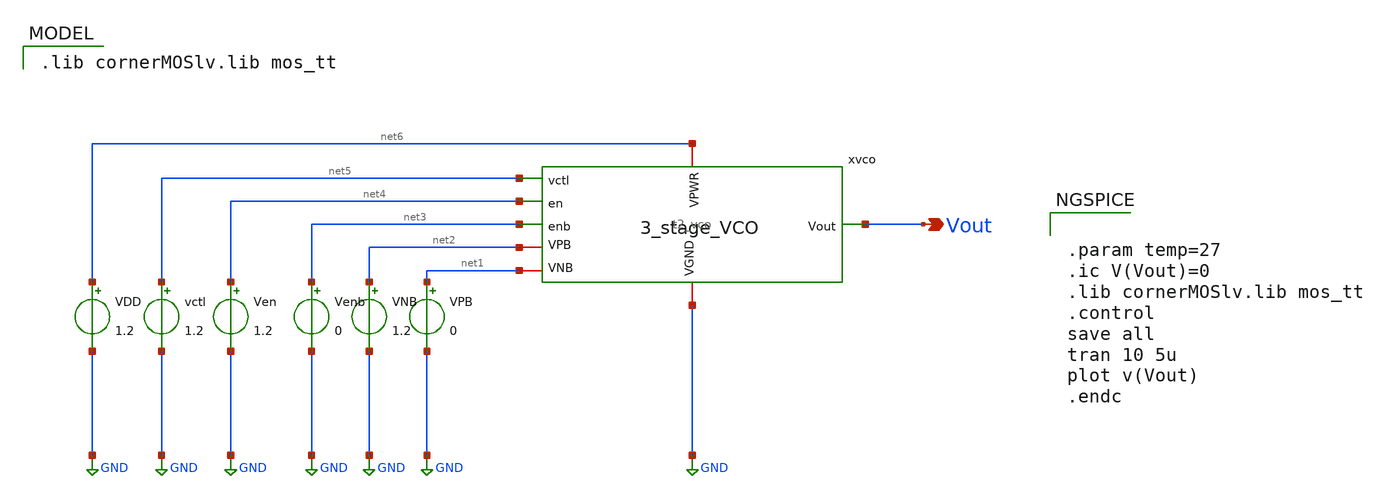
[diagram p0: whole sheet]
** sch_path: Team 2 Design/design_data/xschem/t2_vco_tb.sch
* IHP-GmbH/IHP-Open-PDK/ihp-sg13g2/libs.tech/xschem/sg13g2_stdcells/sg13g2_buf_1.sch:
* Copyright 2023 IHP PDK Authors
* Licensed under the Apache License, Version 2.0 (the "License");
**.subckt t2_vco_tb Vout
*.opin Vout
VDD net6 GND 1.2
vctl net5 GND 1.2
Ven net4 GND 1.2
Venb net3 GND 0
VNB net2 GND 1.2
VPB net1 GND 0
x1 net6 net2 GND net1 Vout net5 net4 net3 t2_vco
**** begin user architecture code
 .lib cornerMOSlv.lib mos_tt



.param temp=27
.ic V(Vout)=0
.lib cornerMOSlv.lib mos_tt
.control
save all
tran 10 5u
plot v(Vout)
.endc


**** end user architecture code
**.ends

* expanding   symbol:  /foss/designs/cmos-pll-ihp-sg13g2/Team 2 Design/design_data/xschem/t2_vco.sym
*+ # of pins=8
** sym_path: Team 2 Design/design_data/xschem/t2_vco.sym
** sch_path: Team 2 Design/design_data/xschem/t2_vco.sch
.subckt t2_vco VPWR VPB VGND VNB Vout vctl en enb
*.iopin VPWR
*.iopin VPB
*.iopin VGND
*.iopin VNB
*.ipin vctl
*.ipin en
*.ipin enb
*.opin Vout
XM1 net1 en VPWR VPB sg13_lv_pmos w=1.0u l=0.15u ng=1 m=1 mm_ok=1
XM2 net1 net1 VPWR VPB sg13_lv_pmos w=3.0u l=0.15u ng=1 m=1 mm_ok=1
XM3 vco_source net1 VPWR VPB sg13_lv_pmos w=3.0u l=0.15u ng=1 m=1 mm_ok=1
XM4 net1 vctl net2 VNB sg13_lv_nmos w=1.5u l=0.15u ng=1 m=1 mm_ok=1
XM5 net2 net2 VGND VNB sg13_lv_nmos w=1.5u l=0.15u ng=1 m=1 mm_ok=1
XM6 vco_sink net2 VGND VNB sg13_lv_nmos w=1.5u l=0.15u ng=1 m=1 mm_ok=1
XM7 net2 enb VGND VNB sg13_lv_nmos w=0.5u l=0.15u ng=1 m=1 mm_ok=1
XM8 vctl enb VGND VNB sg13_lv_nmos w=0.5u l=0.15u ng=1 m=1 mm_ok=1
XM9 net3 enb VGND VNB sg13_lv_nmos w=0.5u l=0.15u ng=1 m=1 mm_ok=1
x2 vco_source net3 net4 vco_sink t2_inverter
x3 vco_source net4 net5 vco_sink t2_inverter
x4 vco_source net5 net3 vco_sink t2_inverter
x1 Vout net3 VPWR VGND sg13g2_buf_1
.ends


* expanding   symbol:  /foss/designs/IHP/Inverter/t2_inverter.sym # of pins=4
** sym_path: Team 2 Design/design_data/xschem/t2_inverter.sym
** sch_path: Team 2 Design/design_data/xschem/t2_inverter.sch
.subckt t2_inverter VP A Y VN
*.iopin VP
*.iopin VN
*.ipin A
*.opin Y
XM2 Y A VP VP sg13_lv_pmos w=0.3u l=0.13u ng=1 m=1 mm_ok=1
XM1 Y A VN VN sg13_lv_nmos w=0.15u l=0.13u ng=1 m=1 mm_ok=1
.ends


* expanding   symbol:  sg13g2_stdcells/sg13g2_buf_1.sym # of pins=2
** sym_path: sg13g2_stdcells/sg13g2_buf_1.sym
** sch_path: sg13g2_stdcells/sg13g2_buf_1.sch
.subckt sg13g2_buf_1 X A VDD VSS
*.ipin A
*.opin X
*.iopin VDD
*.iopin VSS
XM1 net1 A VSS VSS sg13_lv_nmos w=550.00n l=130.00n ng=1 m=1 mm_ok=1
XM2 X net1 VSS VSS sg13_lv_nmos w=740.00n l=130.00n ng=1 m=1 mm_ok=1
XM3 net1 A VDD VDD sg13_lv_pmos w=840.00n l=130.00n ng=1 m=1 mm_ok=1
XM4 X net1 VDD VDD sg13_lv_pmos w=1.12u l=130.00n ng=1 m=1 mm_ok=1
.ends

.GLOBAL GND
.end
